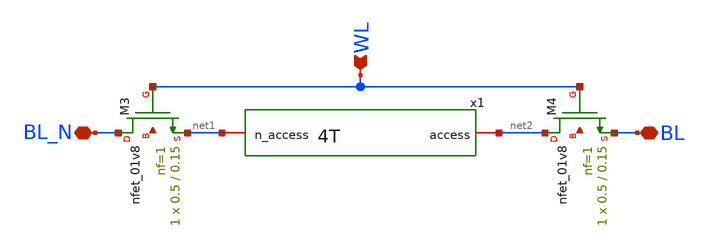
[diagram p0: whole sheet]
** sch_path: analog/schematics/Access_4T.sch
**.subckt Access_4T BL_N BL WL
*.iopin BL_N
*.iopin BL
*.ipin WL
XM3 BL_N WL net1 net3 sky130_fd_pr__nfet_01v8 L=0.15 W=0.5 nf=1 ad='int((nf+1)/2) * W/nf * 0.29' as='int((nf+2)/2) * W/nf * 0.29'
+ pd='2*int((nf+1)/2) * (W/nf + 0.29)' ps='2*int((nf+2)/2) * (W/nf + 0.29)' nrd='0.29 / W' nrs='0.29 / W'
+ sa=0 sb=0 sd=0 mult=1 m=1
XM4 net2 WL BL net4 sky130_fd_pr__nfet_01v8 L=0.15 W=0.5 nf=1 ad='int((nf+1)/2) * W/nf * 0.29' as='int((nf+2)/2) * W/nf * 0.29'
+ pd='2*int((nf+1)/2) * (W/nf + 0.29)' ps='2*int((nf+2)/2) * (W/nf + 0.29)' nrd='0.29 / W' nrs='0.29 / W'
+ sa=0 sb=0 sd=0 mult=1 m=1
x1 net1 net2 4T
**.ends

* expanding   symbol:  4T.sym # of pins=2
** sym_path: analog/schematics/4T.sym
** sch_path: analog/schematics/4T.sch
.subckt 4T access n_access
*.iopin access
*.iopin n_access
XM1 access n_access GND net1 sky130_fd_pr__nfet_01v8 L=0.15 W=1 nf=1 ad='int((nf+1)/2) * W/nf * 0.29'
+ as='int((nf+2)/2) * W/nf * 0.29' pd='2*int((nf+1)/2) * (W/nf + 0.29)' ps='2*int((nf+2)/2) * (W/nf + 0.29)'
+ nrd='0.29 / W' nrs='0.29 / W' sa=0 sb=0 sd=0 mult=1 m=1
XM2 n_access access GND net2 sky130_fd_pr__nfet_01v8 L=0.15 W=1 nf=1 ad='int((nf+1)/2) * W/nf * 0.29'
+ as='int((nf+2)/2) * W/nf * 0.29' pd='2*int((nf+1)/2) * (W/nf + 0.29)' ps='2*int((nf+2)/2) * (W/nf + 0.29)'
+ nrd='0.29 / W' nrs='0.29 / W' sa=0 sb=0 sd=0 mult=1 m=1
XM5 access n_access VDD net3 sky130_fd_pr__pfet_01v8 L=0.15 W=0.5 nf=1 ad='int((nf+1)/2) * W/nf * 0.29'
+ as='int((nf+2)/2) * W/nf * 0.29' pd='2*int((nf+1)/2) * (W/nf + 0.29)' ps='2*int((nf+2)/2) * (W/nf + 0.29)'
+ nrd='0.29 / W' nrs='0.29 / W' sa=0 sb=0 sd=0 mult=1 m=1
XM6 n_access access VDD net4 sky130_fd_pr__pfet_01v8 L=0.15 W=0.5 nf=1 ad='int((nf+1)/2) * W/nf * 0.29'
+ as='int((nf+2)/2) * W/nf * 0.29' pd='2*int((nf+1)/2) * (W/nf + 0.29)' ps='2*int((nf+2)/2) * (W/nf + 0.29)'
+ nrd='0.29 / W' nrs='0.29 / W' sa=0 sb=0 sd=0 mult=1 m=1
.ends

.GLOBAL VDD
.GLOBAL GND
.end
